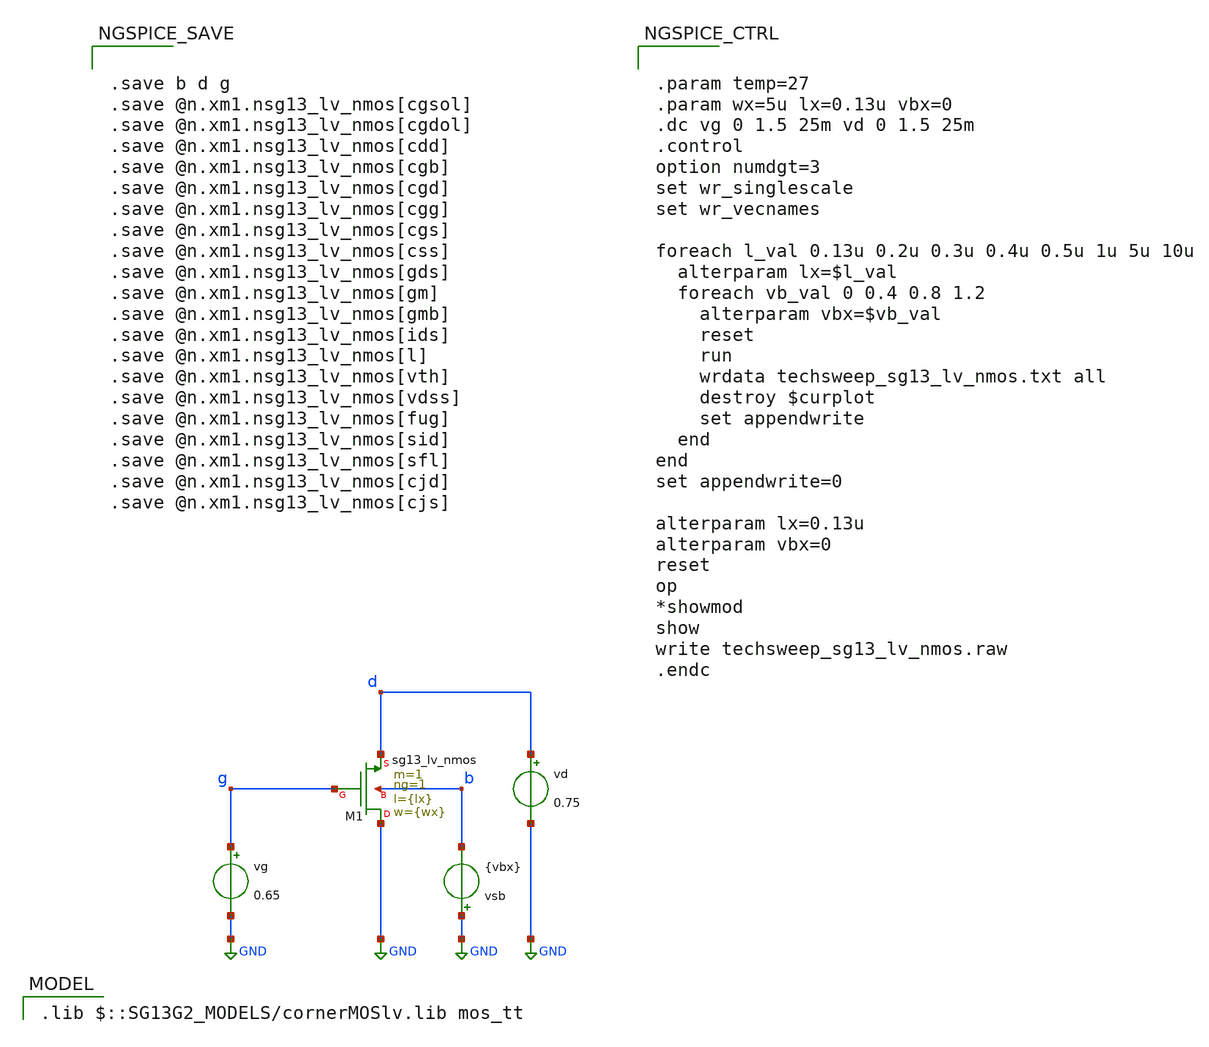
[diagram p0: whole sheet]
** sch_path: xschem/techsweep_sg13g2_lv_nmos.sch
* (c) 2024 Harald Pretl (adapted from Boris Murmann)
**.subckt techsweep_sg13g2_lv_nmos
vg g GND 0.65
vd d GND 0.75
XM1 GND g d b sg13_lv_nmos w={wx} l={lx} ng=1 m=1 mm_ok=1
vsb GND b {vbx}
**** begin user architecture code
 .lib $::SG13G2_MODELS/cornerMOSlv.lib mos_tt



.param temp=27
.param wx=5u lx=0.13u vbx=0
.dc vg 0 1.5 25m vd 0 1.5 25m
.control
option numdgt=3
set wr_singlescale
set wr_vecnames

foreach l_val 0.13u 0.2u 0.3u 0.4u 0.5u 1u 5u 10u
  alterparam lx=$l_val
  foreach vb_val 0 0.4 0.8 1.2
    alterparam vbx=$vb_val
    reset
    run
    wrdata techsweep_sg13_lv_nmos.txt all
    destroy $curplot
    set appendwrite
  end
end
set appendwrite=0

alterparam lx=0.13u
alterparam vbx=0
reset
op
*showmod
show
write techsweep_sg13_lv_nmos.raw
.endc




.save b d g
.save @n.xm1.nsg13_lv_nmos[cgsol]
.save @n.xm1.nsg13_lv_nmos[cgdol]
.save @n.xm1.nsg13_lv_nmos[cdd]
.save @n.xm1.nsg13_lv_nmos[cgb]
.save @n.xm1.nsg13_lv_nmos[cgd]
.save @n.xm1.nsg13_lv_nmos[cgg]
.save @n.xm1.nsg13_lv_nmos[cgs]
.save @n.xm1.nsg13_lv_nmos[css]
.save @n.xm1.nsg13_lv_nmos[gds]
.save @n.xm1.nsg13_lv_nmos[gm]
.save @n.xm1.nsg13_lv_nmos[gmb]
.save @n.xm1.nsg13_lv_nmos[ids]
.save @n.xm1.nsg13_lv_nmos[l]
.save @n.xm1.nsg13_lv_nmos[vth]
.save @n.xm1.nsg13_lv_nmos[vdss]
.save @n.xm1.nsg13_lv_nmos[fug]
.save @n.xm1.nsg13_lv_nmos[sid]
.save @n.xm1.nsg13_lv_nmos[sfl]
.save @n.xm1.nsg13_lv_nmos[cjd]
.save @n.xm1.nsg13_lv_nmos[cjs]


**** end user architecture code
**.ends
.GLOBAL GND
.end
